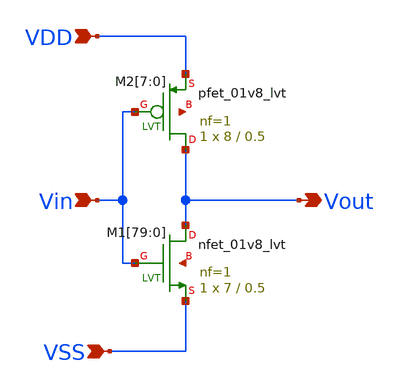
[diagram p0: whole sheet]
** sch_path: design/THESIS_EXP_RO_INVERTER_SKY130A/INV_LVT_v2.sch
**.subckt INV_LVT_v2 VDD VSS Vin Vout
*.ipin VDD
*.ipin VSS
*.ipin Vin
*.opin Vout
XM1[79] Vout Vin VSS net1[79] sky130_fd_pr__nfet_01v8_lvt L=0.5 W=7 nf=1 ad='int((nf+1)/2) * W/nf * 0.29'
+ as='int((nf+2)/2) * W/nf * 0.29' pd='2*int((nf+1)/2) * (W/nf + 0.29)' ps='2*int((nf+2)/2) * (W/nf + 0.29)'
+ nrd='0.29 / W' nrs='0.29 / W' sa=0 sb=0 sd=0 mult=1 m=1
XM1[78] Vout Vin VSS net1[78] sky130_fd_pr__nfet_01v8_lvt L=0.5 W=7 nf=1 ad='int((nf+1)/2) * W/nf * 0.29'
+ as='int((nf+2)/2) * W/nf * 0.29' pd='2*int((nf+1)/2) * (W/nf + 0.29)' ps='2*int((nf+2)/2) * (W/nf + 0.29)'
+ nrd='0.29 / W' nrs='0.29 / W' sa=0 sb=0 sd=0 mult=1 m=1
XM1[77] Vout Vin VSS net1[77] sky130_fd_pr__nfet_01v8_lvt L=0.5 W=7 nf=1 ad='int((nf+1)/2) * W/nf * 0.29'
+ as='int((nf+2)/2) * W/nf * 0.29' pd='2*int((nf+1)/2) * (W/nf + 0.29)' ps='2*int((nf+2)/2) * (W/nf + 0.29)'
+ nrd='0.29 / W' nrs='0.29 / W' sa=0 sb=0 sd=0 mult=1 m=1
XM1[76] Vout Vin VSS net1[76] sky130_fd_pr__nfet_01v8_lvt L=0.5 W=7 nf=1 ad='int((nf+1)/2) * W/nf * 0.29'
+ as='int((nf+2)/2) * W/nf * 0.29' pd='2*int((nf+1)/2) * (W/nf + 0.29)' ps='2*int((nf+2)/2) * (W/nf + 0.29)'
+ nrd='0.29 / W' nrs='0.29 / W' sa=0 sb=0 sd=0 mult=1 m=1
XM1[75] Vout Vin VSS net1[75] sky130_fd_pr__nfet_01v8_lvt L=0.5 W=7 nf=1 ad='int((nf+1)/2) * W/nf * 0.29'
+ as='int((nf+2)/2) * W/nf * 0.29' pd='2*int((nf+1)/2) * (W/nf + 0.29)' ps='2*int((nf+2)/2) * (W/nf + 0.29)'
+ nrd='0.29 / W' nrs='0.29 / W' sa=0 sb=0 sd=0 mult=1 m=1
XM1[74] Vout Vin VSS net1[74] sky130_fd_pr__nfet_01v8_lvt L=0.5 W=7 nf=1 ad='int((nf+1)/2) * W/nf * 0.29'
+ as='int((nf+2)/2) * W/nf * 0.29' pd='2*int((nf+1)/2) * (W/nf + 0.29)' ps='2*int((nf+2)/2) * (W/nf + 0.29)'
+ nrd='0.29 / W' nrs='0.29 / W' sa=0 sb=0 sd=0 mult=1 m=1
XM1[73] Vout Vin VSS net1[73] sky130_fd_pr__nfet_01v8_lvt L=0.5 W=7 nf=1 ad='int((nf+1)/2) * W/nf * 0.29'
+ as='int((nf+2)/2) * W/nf * 0.29' pd='2*int((nf+1)/2) * (W/nf + 0.29)' ps='2*int((nf+2)/2) * (W/nf + 0.29)'
+ nrd='0.29 / W' nrs='0.29 / W' sa=0 sb=0 sd=0 mult=1 m=1
XM1[72] Vout Vin VSS net1[72] sky130_fd_pr__nfet_01v8_lvt L=0.5 W=7 nf=1 ad='int((nf+1)/2) * W/nf * 0.29'
+ as='int((nf+2)/2) * W/nf * 0.29' pd='2*int((nf+1)/2) * (W/nf + 0.29)' ps='2*int((nf+2)/2) * (W/nf + 0.29)'
+ nrd='0.29 / W' nrs='0.29 / W' sa=0 sb=0 sd=0 mult=1 m=1
XM1[71] Vout Vin VSS net1[71] sky130_fd_pr__nfet_01v8_lvt L=0.5 W=7 nf=1 ad='int((nf+1)/2) * W/nf * 0.29'
+ as='int((nf+2)/2) * W/nf * 0.29' pd='2*int((nf+1)/2) * (W/nf + 0.29)' ps='2*int((nf+2)/2) * (W/nf + 0.29)'
+ nrd='0.29 / W' nrs='0.29 / W' sa=0 sb=0 sd=0 mult=1 m=1
XM1[70] Vout Vin VSS net1[70] sky130_fd_pr__nfet_01v8_lvt L=0.5 W=7 nf=1 ad='int((nf+1)/2) * W/nf * 0.29'
+ as='int((nf+2)/2) * W/nf * 0.29' pd='2*int((nf+1)/2) * (W/nf + 0.29)' ps='2*int((nf+2)/2) * (W/nf + 0.29)'
+ nrd='0.29 / W' nrs='0.29 / W' sa=0 sb=0 sd=0 mult=1 m=1
XM1[69] Vout Vin VSS net1[69] sky130_fd_pr__nfet_01v8_lvt L=0.5 W=7 nf=1 ad='int((nf+1)/2) * W/nf * 0.29'
+ as='int((nf+2)/2) * W/nf * 0.29' pd='2*int((nf+1)/2) * (W/nf + 0.29)' ps='2*int((nf+2)/2) * (W/nf + 0.29)'
+ nrd='0.29 / W' nrs='0.29 / W' sa=0 sb=0 sd=0 mult=1 m=1
XM1[68] Vout Vin VSS net1[68] sky130_fd_pr__nfet_01v8_lvt L=0.5 W=7 nf=1 ad='int((nf+1)/2) * W/nf * 0.29'
+ as='int((nf+2)/2) * W/nf * 0.29' pd='2*int((nf+1)/2) * (W/nf + 0.29)' ps='2*int((nf+2)/2) * (W/nf + 0.29)'
+ nrd='0.29 / W' nrs='0.29 / W' sa=0 sb=0 sd=0 mult=1 m=1
XM1[67] Vout Vin VSS net1[67] sky130_fd_pr__nfet_01v8_lvt L=0.5 W=7 nf=1 ad='int((nf+1)/2) * W/nf * 0.29'
+ as='int((nf+2)/2) * W/nf * 0.29' pd='2*int((nf+1)/2) * (W/nf + 0.29)' ps='2*int((nf+2)/2) * (W/nf + 0.29)'
+ nrd='0.29 / W' nrs='0.29 / W' sa=0 sb=0 sd=0 mult=1 m=1
XM1[66] Vout Vin VSS net1[66] sky130_fd_pr__nfet_01v8_lvt L=0.5 W=7 nf=1 ad='int((nf+1)/2) * W/nf * 0.29'
+ as='int((nf+2)/2) * W/nf * 0.29' pd='2*int((nf+1)/2) * (W/nf + 0.29)' ps='2*int((nf+2)/2) * (W/nf + 0.29)'
+ nrd='0.29 / W' nrs='0.29 / W' sa=0 sb=0 sd=0 mult=1 m=1
XM1[65] Vout Vin VSS net1[65] sky130_fd_pr__nfet_01v8_lvt L=0.5 W=7 nf=1 ad='int((nf+1)/2) * W/nf * 0.29'
+ as='int((nf+2)/2) * W/nf * 0.29' pd='2*int((nf+1)/2) * (W/nf + 0.29)' ps='2*int((nf+2)/2) * (W/nf + 0.29)'
+ nrd='0.29 / W' nrs='0.29 / W' sa=0 sb=0 sd=0 mult=1 m=1
XM1[64] Vout Vin VSS net1[64] sky130_fd_pr__nfet_01v8_lvt L=0.5 W=7 nf=1 ad='int((nf+1)/2) * W/nf * 0.29'
+ as='int((nf+2)/2) * W/nf * 0.29' pd='2*int((nf+1)/2) * (W/nf + 0.29)' ps='2*int((nf+2)/2) * (W/nf + 0.29)'
+ nrd='0.29 / W' nrs='0.29 / W' sa=0 sb=0 sd=0 mult=1 m=1
XM1[63] Vout Vin VSS net1[63] sky130_fd_pr__nfet_01v8_lvt L=0.5 W=7 nf=1 ad='int((nf+1)/2) * W/nf * 0.29'
+ as='int((nf+2)/2) * W/nf * 0.29' pd='2*int((nf+1)/2) * (W/nf + 0.29)' ps='2*int((nf+2)/2) * (W/nf + 0.29)'
+ nrd='0.29 / W' nrs='0.29 / W' sa=0 sb=0 sd=0 mult=1 m=1
XM1[62] Vout Vin VSS net1[62] sky130_fd_pr__nfet_01v8_lvt L=0.5 W=7 nf=1 ad='int((nf+1)/2) * W/nf * 0.29'
+ as='int((nf+2)/2) * W/nf * 0.29' pd='2*int((nf+1)/2) * (W/nf + 0.29)' ps='2*int((nf+2)/2) * (W/nf + 0.29)'
+ nrd='0.29 / W' nrs='0.29 / W' sa=0 sb=0 sd=0 mult=1 m=1
XM1[61] Vout Vin VSS net1[61] sky130_fd_pr__nfet_01v8_lvt L=0.5 W=7 nf=1 ad='int((nf+1)/2) * W/nf * 0.29'
+ as='int((nf+2)/2) * W/nf * 0.29' pd='2*int((nf+1)/2) * (W/nf + 0.29)' ps='2*int((nf+2)/2) * (W/nf + 0.29)'
+ nrd='0.29 / W' nrs='0.29 / W' sa=0 sb=0 sd=0 mult=1 m=1
XM1[60] Vout Vin VSS net1[60] sky130_fd_pr__nfet_01v8_lvt L=0.5 W=7 nf=1 ad='int((nf+1)/2) * W/nf * 0.29'
+ as='int((nf+2)/2) * W/nf * 0.29' pd='2*int((nf+1)/2) * (W/nf + 0.29)' ps='2*int((nf+2)/2) * (W/nf + 0.29)'
+ nrd='0.29 / W' nrs='0.29 / W' sa=0 sb=0 sd=0 mult=1 m=1
XM1[59] Vout Vin VSS net1[59] sky130_fd_pr__nfet_01v8_lvt L=0.5 W=7 nf=1 ad='int((nf+1)/2) * W/nf * 0.29'
+ as='int((nf+2)/2) * W/nf * 0.29' pd='2*int((nf+1)/2) * (W/nf + 0.29)' ps='2*int((nf+2)/2) * (W/nf + 0.29)'
+ nrd='0.29 / W' nrs='0.29 / W' sa=0 sb=0 sd=0 mult=1 m=1
XM1[58] Vout Vin VSS net1[58] sky130_fd_pr__nfet_01v8_lvt L=0.5 W=7 nf=1 ad='int((nf+1)/2) * W/nf * 0.29'
+ as='int((nf+2)/2) * W/nf * 0.29' pd='2*int((nf+1)/2) * (W/nf + 0.29)' ps='2*int((nf+2)/2) * (W/nf + 0.29)'
+ nrd='0.29 / W' nrs='0.29 / W' sa=0 sb=0 sd=0 mult=1 m=1
XM1[57] Vout Vin VSS net1[57] sky130_fd_pr__nfet_01v8_lvt L=0.5 W=7 nf=1 ad='int((nf+1)/2) * W/nf * 0.29'
+ as='int((nf+2)/2) * W/nf * 0.29' pd='2*int((nf+1)/2) * (W/nf + 0.29)' ps='2*int((nf+2)/2) * (W/nf + 0.29)'
+ nrd='0.29 / W' nrs='0.29 / W' sa=0 sb=0 sd=0 mult=1 m=1
XM1[56] Vout Vin VSS net1[56] sky130_fd_pr__nfet_01v8_lvt L=0.5 W=7 nf=1 ad='int((nf+1)/2) * W/nf * 0.29'
+ as='int((nf+2)/2) * W/nf * 0.29' pd='2*int((nf+1)/2) * (W/nf + 0.29)' ps='2*int((nf+2)/2) * (W/nf + 0.29)'
+ nrd='0.29 / W' nrs='0.29 / W' sa=0 sb=0 sd=0 mult=1 m=1
XM1[55] Vout Vin VSS net1[55] sky130_fd_pr__nfet_01v8_lvt L=0.5 W=7 nf=1 ad='int((nf+1)/2) * W/nf * 0.29'
+ as='int((nf+2)/2) * W/nf * 0.29' pd='2*int((nf+1)/2) * (W/nf + 0.29)' ps='2*int((nf+2)/2) * (W/nf + 0.29)'
+ nrd='0.29 / W' nrs='0.29 / W' sa=0 sb=0 sd=0 mult=1 m=1
XM1[54] Vout Vin VSS net1[54] sky130_fd_pr__nfet_01v8_lvt L=0.5 W=7 nf=1 ad='int((nf+1)/2) * W/nf * 0.29'
+ as='int((nf+2)/2) * W/nf * 0.29' pd='2*int((nf+1)/2) * (W/nf + 0.29)' ps='2*int((nf+2)/2) * (W/nf + 0.29)'
+ nrd='0.29 / W' nrs='0.29 / W' sa=0 sb=0 sd=0 mult=1 m=1
XM1[53] Vout Vin VSS net1[53] sky130_fd_pr__nfet_01v8_lvt L=0.5 W=7 nf=1 ad='int((nf+1)/2) * W/nf * 0.29'
+ as='int((nf+2)/2) * W/nf * 0.29' pd='2*int((nf+1)/2) * (W/nf + 0.29)' ps='2*int((nf+2)/2) * (W/nf + 0.29)'
+ nrd='0.29 / W' nrs='0.29 / W' sa=0 sb=0 sd=0 mult=1 m=1
XM1[52] Vout Vin VSS net1[52] sky130_fd_pr__nfet_01v8_lvt L=0.5 W=7 nf=1 ad='int((nf+1)/2) * W/nf * 0.29'
+ as='int((nf+2)/2) * W/nf * 0.29' pd='2*int((nf+1)/2) * (W/nf + 0.29)' ps='2*int((nf+2)/2) * (W/nf + 0.29)'
+ nrd='0.29 / W' nrs='0.29 / W' sa=0 sb=0 sd=0 mult=1 m=1
XM1[51] Vout Vin VSS net1[51] sky130_fd_pr__nfet_01v8_lvt L=0.5 W=7 nf=1 ad='int((nf+1)/2) * W/nf * 0.29'
+ as='int((nf+2)/2) * W/nf * 0.29' pd='2*int((nf+1)/2) * (W/nf + 0.29)' ps='2*int((nf+2)/2) * (W/nf + 0.29)'
+ nrd='0.29 / W' nrs='0.29 / W' sa=0 sb=0 sd=0 mult=1 m=1
XM1[50] Vout Vin VSS net1[50] sky130_fd_pr__nfet_01v8_lvt L=0.5 W=7 nf=1 ad='int((nf+1)/2) * W/nf * 0.29'
+ as='int((nf+2)/2) * W/nf * 0.29' pd='2*int((nf+1)/2) * (W/nf + 0.29)' ps='2*int((nf+2)/2) * (W/nf + 0.29)'
+ nrd='0.29 / W' nrs='0.29 / W' sa=0 sb=0 sd=0 mult=1 m=1
XM1[49] Vout Vin VSS net1[49] sky130_fd_pr__nfet_01v8_lvt L=0.5 W=7 nf=1 ad='int((nf+1)/2) * W/nf * 0.29'
+ as='int((nf+2)/2) * W/nf * 0.29' pd='2*int((nf+1)/2) * (W/nf + 0.29)' ps='2*int((nf+2)/2) * (W/nf + 0.29)'
+ nrd='0.29 / W' nrs='0.29 / W' sa=0 sb=0 sd=0 mult=1 m=1
XM1[48] Vout Vin VSS net1[48] sky130_fd_pr__nfet_01v8_lvt L=0.5 W=7 nf=1 ad='int((nf+1)/2) * W/nf * 0.29'
+ as='int((nf+2)/2) * W/nf * 0.29' pd='2*int((nf+1)/2) * (W/nf + 0.29)' ps='2*int((nf+2)/2) * (W/nf + 0.29)'
+ nrd='0.29 / W' nrs='0.29 / W' sa=0 sb=0 sd=0 mult=1 m=1
XM1[47] Vout Vin VSS net1[47] sky130_fd_pr__nfet_01v8_lvt L=0.5 W=7 nf=1 ad='int((nf+1)/2) * W/nf * 0.29'
+ as='int((nf+2)/2) * W/nf * 0.29' pd='2*int((nf+1)/2) * (W/nf + 0.29)' ps='2*int((nf+2)/2) * (W/nf + 0.29)'
+ nrd='0.29 / W' nrs='0.29 / W' sa=0 sb=0 sd=0 mult=1 m=1
XM1[46] Vout Vin VSS net1[46] sky130_fd_pr__nfet_01v8_lvt L=0.5 W=7 nf=1 ad='int((nf+1)/2) * W/nf * 0.29'
+ as='int((nf+2)/2) * W/nf * 0.29' pd='2*int((nf+1)/2) * (W/nf + 0.29)' ps='2*int((nf+2)/2) * (W/nf + 0.29)'
+ nrd='0.29 / W' nrs='0.29 / W' sa=0 sb=0 sd=0 mult=1 m=1
XM1[45] Vout Vin VSS net1[45] sky130_fd_pr__nfet_01v8_lvt L=0.5 W=7 nf=1 ad='int((nf+1)/2) * W/nf * 0.29'
+ as='int((nf+2)/2) * W/nf * 0.29' pd='2*int((nf+1)/2) * (W/nf + 0.29)' ps='2*int((nf+2)/2) * (W/nf + 0.29)'
+ nrd='0.29 / W' nrs='0.29 / W' sa=0 sb=0 sd=0 mult=1 m=1
XM1[44] Vout Vin VSS net1[44] sky130_fd_pr__nfet_01v8_lvt L=0.5 W=7 nf=1 ad='int((nf+1)/2) * W/nf * 0.29'
+ as='int((nf+2)/2) * W/nf * 0.29' pd='2*int((nf+1)/2) * (W/nf + 0.29)' ps='2*int((nf+2)/2) * (W/nf + 0.29)'
+ nrd='0.29 / W' nrs='0.29 / W' sa=0 sb=0 sd=0 mult=1 m=1
XM1[43] Vout Vin VSS net1[43] sky130_fd_pr__nfet_01v8_lvt L=0.5 W=7 nf=1 ad='int((nf+1)/2) * W/nf * 0.29'
+ as='int((nf+2)/2) * W/nf * 0.29' pd='2*int((nf+1)/2) * (W/nf + 0.29)' ps='2*int((nf+2)/2) * (W/nf + 0.29)'
+ nrd='0.29 / W' nrs='0.29 / W' sa=0 sb=0 sd=0 mult=1 m=1
XM1[42] Vout Vin VSS net1[42] sky130_fd_pr__nfet_01v8_lvt L=0.5 W=7 nf=1 ad='int((nf+1)/2) * W/nf * 0.29'
+ as='int((nf+2)/2) * W/nf * 0.29' pd='2*int((nf+1)/2) * (W/nf + 0.29)' ps='2*int((nf+2)/2) * (W/nf + 0.29)'
+ nrd='0.29 / W' nrs='0.29 / W' sa=0 sb=0 sd=0 mult=1 m=1
XM1[41] Vout Vin VSS net1[41] sky130_fd_pr__nfet_01v8_lvt L=0.5 W=7 nf=1 ad='int((nf+1)/2) * W/nf * 0.29'
+ as='int((nf+2)/2) * W/nf * 0.29' pd='2*int((nf+1)/2) * (W/nf + 0.29)' ps='2*int((nf+2)/2) * (W/nf + 0.29)'
+ nrd='0.29 / W' nrs='0.29 / W' sa=0 sb=0 sd=0 mult=1 m=1
XM1[40] Vout Vin VSS net1[40] sky130_fd_pr__nfet_01v8_lvt L=0.5 W=7 nf=1 ad='int((nf+1)/2) * W/nf * 0.29'
+ as='int((nf+2)/2) * W/nf * 0.29' pd='2*int((nf+1)/2) * (W/nf + 0.29)' ps='2*int((nf+2)/2) * (W/nf + 0.29)'
+ nrd='0.29 / W' nrs='0.29 / W' sa=0 sb=0 sd=0 mult=1 m=1
XM1[39] Vout Vin VSS net1[39] sky130_fd_pr__nfet_01v8_lvt L=0.5 W=7 nf=1 ad='int((nf+1)/2) * W/nf * 0.29'
+ as='int((nf+2)/2) * W/nf * 0.29' pd='2*int((nf+1)/2) * (W/nf + 0.29)' ps='2*int((nf+2)/2) * (W/nf + 0.29)'
+ nrd='0.29 / W' nrs='0.29 / W' sa=0 sb=0 sd=0 mult=1 m=1
XM1[38] Vout Vin VSS net1[38] sky130_fd_pr__nfet_01v8_lvt L=0.5 W=7 nf=1 ad='int((nf+1)/2) * W/nf * 0.29'
+ as='int((nf+2)/2) * W/nf * 0.29' pd='2*int((nf+1)/2) * (W/nf + 0.29)' ps='2*int((nf+2)/2) * (W/nf + 0.29)'
+ nrd='0.29 / W' nrs='0.29 / W' sa=0 sb=0 sd=0 mult=1 m=1
XM1[37] Vout Vin VSS net1[37] sky130_fd_pr__nfet_01v8_lvt L=0.5 W=7 nf=1 ad='int((nf+1)/2) * W/nf * 0.29'
+ as='int((nf+2)/2) * W/nf * 0.29' pd='2*int((nf+1)/2) * (W/nf + 0.29)' ps='2*int((nf+2)/2) * (W/nf + 0.29)'
+ nrd='0.29 / W' nrs='0.29 / W' sa=0 sb=0 sd=0 mult=1 m=1
XM1[36] Vout Vin VSS net1[36] sky130_fd_pr__nfet_01v8_lvt L=0.5 W=7 nf=1 ad='int((nf+1)/2) * W/nf * 0.29'
+ as='int((nf+2)/2) * W/nf * 0.29' pd='2*int((nf+1)/2) * (W/nf + 0.29)' ps='2*int((nf+2)/2) * (W/nf + 0.29)'
+ nrd='0.29 / W' nrs='0.29 / W' sa=0 sb=0 sd=0 mult=1 m=1
XM1[35] Vout Vin VSS net1[35] sky130_fd_pr__nfet_01v8_lvt L=0.5 W=7 nf=1 ad='int((nf+1)/2) * W/nf * 0.29'
+ as='int((nf+2)/2) * W/nf * 0.29' pd='2*int((nf+1)/2) * (W/nf + 0.29)' ps='2*int((nf+2)/2) * (W/nf + 0.29)'
+ nrd='0.29 / W' nrs='0.29 / W' sa=0 sb=0 sd=0 mult=1 m=1
XM1[34] Vout Vin VSS net1[34] sky130_fd_pr__nfet_01v8_lvt L=0.5 W=7 nf=1 ad='int((nf+1)/2) * W/nf * 0.29'
+ as='int((nf+2)/2) * W/nf * 0.29' pd='2*int((nf+1)/2) * (W/nf + 0.29)' ps='2*int((nf+2)/2) * (W/nf + 0.29)'
+ nrd='0.29 / W' nrs='0.29 / W' sa=0 sb=0 sd=0 mult=1 m=1
XM1[33] Vout Vin VSS net1[33] sky130_fd_pr__nfet_01v8_lvt L=0.5 W=7 nf=1 ad='int((nf+1)/2) * W/nf * 0.29'
+ as='int((nf+2)/2) * W/nf * 0.29' pd='2*int((nf+1)/2) * (W/nf + 0.29)' ps='2*int((nf+2)/2) * (W/nf + 0.29)'
+ nrd='0.29 / W' nrs='0.29 / W' sa=0 sb=0 sd=0 mult=1 m=1
XM1[32] Vout Vin VSS net1[32] sky130_fd_pr__nfet_01v8_lvt L=0.5 W=7 nf=1 ad='int((nf+1)/2) * W/nf * 0.29'
+ as='int((nf+2)/2) * W/nf * 0.29' pd='2*int((nf+1)/2) * (W/nf + 0.29)' ps='2*int((nf+2)/2) * (W/nf + 0.29)'
+ nrd='0.29 / W' nrs='0.29 / W' sa=0 sb=0 sd=0 mult=1 m=1
XM1[31] Vout Vin VSS net1[31] sky130_fd_pr__nfet_01v8_lvt L=0.5 W=7 nf=1 ad='int((nf+1)/2) * W/nf * 0.29'
+ as='int((nf+2)/2) * W/nf * 0.29' pd='2*int((nf+1)/2) * (W/nf + 0.29)' ps='2*int((nf+2)/2) * (W/nf + 0.29)'
+ nrd='0.29 / W' nrs='0.29 / W' sa=0 sb=0 sd=0 mult=1 m=1
XM1[30] Vout Vin VSS net1[30] sky130_fd_pr__nfet_01v8_lvt L=0.5 W=7 nf=1 ad='int((nf+1)/2) * W/nf * 0.29'
+ as='int((nf+2)/2) * W/nf * 0.29' pd='2*int((nf+1)/2) * (W/nf + 0.29)' ps='2*int((nf+2)/2) * (W/nf + 0.29)'
+ nrd='0.29 / W' nrs='0.29 / W' sa=0 sb=0 sd=0 mult=1 m=1
XM1[29] Vout Vin VSS net1[29] sky130_fd_pr__nfet_01v8_lvt L=0.5 W=7 nf=1 ad='int((nf+1)/2) * W/nf * 0.29'
+ as='int((nf+2)/2) * W/nf * 0.29' pd='2*int((nf+1)/2) * (W/nf + 0.29)' ps='2*int((nf+2)/2) * (W/nf + 0.29)'
+ nrd='0.29 / W' nrs='0.29 / W' sa=0 sb=0 sd=0 mult=1 m=1
XM1[28] Vout Vin VSS net1[28] sky130_fd_pr__nfet_01v8_lvt L=0.5 W=7 nf=1 ad='int((nf+1)/2) * W/nf * 0.29'
+ as='int((nf+2)/2) * W/nf * 0.29' pd='2*int((nf+1)/2) * (W/nf + 0.29)' ps='2*int((nf+2)/2) * (W/nf + 0.29)'
+ nrd='0.29 / W' nrs='0.29 / W' sa=0 sb=0 sd=0 mult=1 m=1
XM1[27] Vout Vin VSS net1[27] sky130_fd_pr__nfet_01v8_lvt L=0.5 W=7 nf=1 ad='int((nf+1)/2) * W/nf * 0.29'
+ as='int((nf+2)/2) * W/nf * 0.29' pd='2*int((nf+1)/2) * (W/nf + 0.29)' ps='2*int((nf+2)/2) * (W/nf + 0.29)'
+ nrd='0.29 / W' nrs='0.29 / W' sa=0 sb=0 sd=0 mult=1 m=1
XM1[26] Vout Vin VSS net1[26] sky130_fd_pr__nfet_01v8_lvt L=0.5 W=7 nf=1 ad='int((nf+1)/2) * W/nf * 0.29'
+ as='int((nf+2)/2) * W/nf * 0.29' pd='2*int((nf+1)/2) * (W/nf + 0.29)' ps='2*int((nf+2)/2) * (W/nf + 0.29)'
+ nrd='0.29 / W' nrs='0.29 / W' sa=0 sb=0 sd=0 mult=1 m=1
XM1[25] Vout Vin VSS net1[25] sky130_fd_pr__nfet_01v8_lvt L=0.5 W=7 nf=1 ad='int((nf+1)/2) * W/nf * 0.29'
+ as='int((nf+2)/2) * W/nf * 0.29' pd='2*int((nf+1)/2) * (W/nf + 0.29)' ps='2*int((nf+2)/2) * (W/nf + 0.29)'
+ nrd='0.29 / W' nrs='0.29 / W' sa=0 sb=0 sd=0 mult=1 m=1
XM1[24] Vout Vin VSS net1[24] sky130_fd_pr__nfet_01v8_lvt L=0.5 W=7 nf=1 ad='int((nf+1)/2) * W/nf * 0.29'
+ as='int((nf+2)/2) * W/nf * 0.29' pd='2*int((nf+1)/2) * (W/nf + 0.29)' ps='2*int((nf+2)/2) * (W/nf + 0.29)'
+ nrd='0.29 / W' nrs='0.29 / W' sa=0 sb=0 sd=0 mult=1 m=1
XM1[23] Vout Vin VSS net1[23] sky130_fd_pr__nfet_01v8_lvt L=0.5 W=7 nf=1 ad='int((nf+1)/2) * W/nf * 0.29'
+ as='int((nf+2)/2) * W/nf * 0.29' pd='2*int((nf+1)/2) * (W/nf + 0.29)' ps='2*int((nf+2)/2) * (W/nf + 0.29)'
+ nrd='0.29 / W' nrs='0.29 / W' sa=0 sb=0 sd=0 mult=1 m=1
XM1[22] Vout Vin VSS net1[22] sky130_fd_pr__nfet_01v8_lvt L=0.5 W=7 nf=1 ad='int((nf+1)/2) * W/nf * 0.29'
+ as='int((nf+2)/2) * W/nf * 0.29' pd='2*int((nf+1)/2) * (W/nf + 0.29)' ps='2*int((nf+2)/2) * (W/nf + 0.29)'
+ nrd='0.29 / W' nrs='0.29 / W' sa=0 sb=0 sd=0 mult=1 m=1
XM1[21] Vout Vin VSS net1[21] sky130_fd_pr__nfet_01v8_lvt L=0.5 W=7 nf=1 ad='int((nf+1)/2) * W/nf * 0.29'
+ as='int((nf+2)/2) * W/nf * 0.29' pd='2*int((nf+1)/2) * (W/nf + 0.29)' ps='2*int((nf+2)/2) * (W/nf + 0.29)'
+ nrd='0.29 / W' nrs='0.29 / W' sa=0 sb=0 sd=0 mult=1 m=1
XM1[20] Vout Vin VSS net1[20] sky130_fd_pr__nfet_01v8_lvt L=0.5 W=7 nf=1 ad='int((nf+1)/2) * W/nf * 0.29'
+ as='int((nf+2)/2) * W/nf * 0.29' pd='2*int((nf+1)/2) * (W/nf + 0.29)' ps='2*int((nf+2)/2) * (W/nf + 0.29)'
+ nrd='0.29 / W' nrs='0.29 / W' sa=0 sb=0 sd=0 mult=1 m=1
XM1[19] Vout Vin VSS net1[19] sky130_fd_pr__nfet_01v8_lvt L=0.5 W=7 nf=1 ad='int((nf+1)/2) * W/nf * 0.29'
+ as='int((nf+2)/2) * W/nf * 0.29' pd='2*int((nf+1)/2) * (W/nf + 0.29)' ps='2*int((nf+2)/2) * (W/nf + 0.29)'
+ nrd='0.29 / W' nrs='0.29 / W' sa=0 sb=0 sd=0 mult=1 m=1
XM1[18] Vout Vin VSS net1[18] sky130_fd_pr__nfet_01v8_lvt L=0.5 W=7 nf=1 ad='int((nf+1)/2) * W/nf * 0.29'
+ as='int((nf+2)/2) * W/nf * 0.29' pd='2*int((nf+1)/2) * (W/nf + 0.29)' ps='2*int((nf+2)/2) * (W/nf + 0.29)'
+ nrd='0.29 / W' nrs='0.29 / W' sa=0 sb=0 sd=0 mult=1 m=1
XM1[17] Vout Vin VSS net1[17] sky130_fd_pr__nfet_01v8_lvt L=0.5 W=7 nf=1 ad='int((nf+1)/2) * W/nf * 0.29'
+ as='int((nf+2)/2) * W/nf * 0.29' pd='2*int((nf+1)/2) * (W/nf + 0.29)' ps='2*int((nf+2)/2) * (W/nf + 0.29)'
+ nrd='0.29 / W' nrs='0.29 / W' sa=0 sb=0 sd=0 mult=1 m=1
XM1[16] Vout Vin VSS net1[16] sky130_fd_pr__nfet_01v8_lvt L=0.5 W=7 nf=1 ad='int((nf+1)/2) * W/nf * 0.29'
+ as='int((nf+2)/2) * W/nf * 0.29' pd='2*int((nf+1)/2) * (W/nf + 0.29)' ps='2*int((nf+2)/2) * (W/nf + 0.29)'
+ nrd='0.29 / W' nrs='0.29 / W' sa=0 sb=0 sd=0 mult=1 m=1
XM1[15] Vout Vin VSS net1[15] sky130_fd_pr__nfet_01v8_lvt L=0.5 W=7 nf=1 ad='int((nf+1)/2) * W/nf * 0.29'
+ as='int((nf+2)/2) * W/nf * 0.29' pd='2*int((nf+1)/2) * (W/nf + 0.29)' ps='2*int((nf+2)/2) * (W/nf + 0.29)'
+ nrd='0.29 / W' nrs='0.29 / W' sa=0 sb=0 sd=0 mult=1 m=1
XM1[14] Vout Vin VSS net1[14] sky130_fd_pr__nfet_01v8_lvt L=0.5 W=7 nf=1 ad='int((nf+1)/2) * W/nf * 0.29'
+ as='int((nf+2)/2) * W/nf * 0.29' pd='2*int((nf+1)/2) * (W/nf + 0.29)' ps='2*int((nf+2)/2) * (W/nf + 0.29)'
+ nrd='0.29 / W' nrs='0.29 / W' sa=0 sb=0 sd=0 mult=1 m=1
XM1[13] Vout Vin VSS net1[13] sky130_fd_pr__nfet_01v8_lvt L=0.5 W=7 nf=1 ad='int((nf+1)/2) * W/nf * 0.29'
+ as='int((nf+2)/2) * W/nf * 0.29' pd='2*int((nf+1)/2) * (W/nf + 0.29)' ps='2*int((nf+2)/2) * (W/nf + 0.29)'
+ nrd='0.29 / W' nrs='0.29 / W' sa=0 sb=0 sd=0 mult=1 m=1
XM1[12] Vout Vin VSS net1[12] sky130_fd_pr__nfet_01v8_lvt L=0.5 W=7 nf=1 ad='int((nf+1)/2) * W/nf * 0.29'
+ as='int((nf+2)/2) * W/nf * 0.29' pd='2*int((nf+1)/2) * (W/nf + 0.29)' ps='2*int((nf+2)/2) * (W/nf + 0.29)'
+ nrd='0.29 / W' nrs='0.29 / W' sa=0 sb=0 sd=0 mult=1 m=1
XM1[11] Vout Vin VSS net1[11] sky130_fd_pr__nfet_01v8_lvt L=0.5 W=7 nf=1 ad='int((nf+1)/2) * W/nf * 0.29'
+ as='int((nf+2)/2) * W/nf * 0.29' pd='2*int((nf+1)/2) * (W/nf + 0.29)' ps='2*int((nf+2)/2) * (W/nf + 0.29)'
+ nrd='0.29 / W' nrs='0.29 / W' sa=0 sb=0 sd=0 mult=1 m=1
XM1[10] Vout Vin VSS net1[10] sky130_fd_pr__nfet_01v8_lvt L=0.5 W=7 nf=1 ad='int((nf+1)/2) * W/nf * 0.29'
+ as='int((nf+2)/2) * W/nf * 0.29' pd='2*int((nf+1)/2) * (W/nf + 0.29)' ps='2*int((nf+2)/2) * (W/nf + 0.29)'
+ nrd='0.29 / W' nrs='0.29 / W' sa=0 sb=0 sd=0 mult=1 m=1
XM1[9] Vout Vin VSS net1[9] sky130_fd_pr__nfet_01v8_lvt L=0.5 W=7 nf=1 ad='int((nf+1)/2) * W/nf * 0.29'
+ as='int((nf+2)/2) * W/nf * 0.29' pd='2*int((nf+1)/2) * (W/nf + 0.29)' ps='2*int((nf+2)/2) * (W/nf + 0.29)'
+ nrd='0.29 / W' nrs='0.29 / W' sa=0 sb=0 sd=0 mult=1 m=1
XM1[8] Vout Vin VSS net1[8] sky130_fd_pr__nfet_01v8_lvt L=0.5 W=7 nf=1 ad='int((nf+1)/2) * W/nf * 0.29'
+ as='int((nf+2)/2) * W/nf * 0.29' pd='2*int((nf+1)/2) * (W/nf + 0.29)' ps='2*int((nf+2)/2) * (W/nf + 0.29)'
+ nrd='0.29 / W' nrs='0.29 / W' sa=0 sb=0 sd=0 mult=1 m=1
XM1[7] Vout Vin VSS net1[7] sky130_fd_pr__nfet_01v8_lvt L=0.5 W=7 nf=1 ad='int((nf+1)/2) * W/nf * 0.29'
+ as='int((nf+2)/2) * W/nf * 0.29' pd='2*int((nf+1)/2) * (W/nf + 0.29)' ps='2*int((nf+2)/2) * (W/nf + 0.29)'
+ nrd='0.29 / W' nrs='0.29 / W' sa=0 sb=0 sd=0 mult=1 m=1
XM1[6] Vout Vin VSS net1[6] sky130_fd_pr__nfet_01v8_lvt L=0.5 W=7 nf=1 ad='int((nf+1)/2) * W/nf * 0.29'
+ as='int((nf+2)/2) * W/nf * 0.29' pd='2*int((nf+1)/2) * (W/nf + 0.29)' ps='2*int((nf+2)/2) * (W/nf + 0.29)'
+ nrd='0.29 / W' nrs='0.29 / W' sa=0 sb=0 sd=0 mult=1 m=1
XM1[5] Vout Vin VSS net1[5] sky130_fd_pr__nfet_01v8_lvt L=0.5 W=7 nf=1 ad='int((nf+1)/2) * W/nf * 0.29'
+ as='int((nf+2)/2) * W/nf * 0.29' pd='2*int((nf+1)/2) * (W/nf + 0.29)' ps='2*int((nf+2)/2) * (W/nf + 0.29)'
+ nrd='0.29 / W' nrs='0.29 / W' sa=0 sb=0 sd=0 mult=1 m=1
XM1[4] Vout Vin VSS net1[4] sky130_fd_pr__nfet_01v8_lvt L=0.5 W=7 nf=1 ad='int((nf+1)/2) * W/nf * 0.29'
+ as='int((nf+2)/2) * W/nf * 0.29' pd='2*int((nf+1)/2) * (W/nf + 0.29)' ps='2*int((nf+2)/2) * (W/nf + 0.29)'
+ nrd='0.29 / W' nrs='0.29 / W' sa=0 sb=0 sd=0 mult=1 m=1
XM1[3] Vout Vin VSS net1[3] sky130_fd_pr__nfet_01v8_lvt L=0.5 W=7 nf=1 ad='int((nf+1)/2) * W/nf * 0.29'
+ as='int((nf+2)/2) * W/nf * 0.29' pd='2*int((nf+1)/2) * (W/nf + 0.29)' ps='2*int((nf+2)/2) * (W/nf + 0.29)'
+ nrd='0.29 / W' nrs='0.29 / W' sa=0 sb=0 sd=0 mult=1 m=1
XM1[2] Vout Vin VSS net1[2] sky130_fd_pr__nfet_01v8_lvt L=0.5 W=7 nf=1 ad='int((nf+1)/2) * W/nf * 0.29'
+ as='int((nf+2)/2) * W/nf * 0.29' pd='2*int((nf+1)/2) * (W/nf + 0.29)' ps='2*int((nf+2)/2) * (W/nf + 0.29)'
+ nrd='0.29 / W' nrs='0.29 / W' sa=0 sb=0 sd=0 mult=1 m=1
XM1[1] Vout Vin VSS net1[1] sky130_fd_pr__nfet_01v8_lvt L=0.5 W=7 nf=1 ad='int((nf+1)/2) * W/nf * 0.29'
+ as='int((nf+2)/2) * W/nf * 0.29' pd='2*int((nf+1)/2) * (W/nf + 0.29)' ps='2*int((nf+2)/2) * (W/nf + 0.29)'
+ nrd='0.29 / W' nrs='0.29 / W' sa=0 sb=0 sd=0 mult=1 m=1
XM1[0] Vout Vin VSS net1[0] sky130_fd_pr__nfet_01v8_lvt L=0.5 W=7 nf=1 ad='int((nf+1)/2) * W/nf * 0.29'
+ as='int((nf+2)/2) * W/nf * 0.29' pd='2*int((nf+1)/2) * (W/nf + 0.29)' ps='2*int((nf+2)/2) * (W/nf + 0.29)'
+ nrd='0.29 / W' nrs='0.29 / W' sa=0 sb=0 sd=0 mult=1 m=1
XM2[7] Vout Vin VDD net2[7] sky130_fd_pr__pfet_01v8_lvt L=0.5 W=8 nf=1 ad='int((nf+1)/2) * W/nf * 0.29'
+ as='int((nf+2)/2) * W/nf * 0.29' pd='2*int((nf+1)/2) * (W/nf + 0.29)' ps='2*int((nf+2)/2) * (W/nf + 0.29)'
+ nrd='0.29 / W' nrs='0.29 / W' sa=0 sb=0 sd=0 mult=1 m=1
XM2[6] Vout Vin VDD net2[6] sky130_fd_pr__pfet_01v8_lvt L=0.5 W=8 nf=1 ad='int((nf+1)/2) * W/nf * 0.29'
+ as='int((nf+2)/2) * W/nf * 0.29' pd='2*int((nf+1)/2) * (W/nf + 0.29)' ps='2*int((nf+2)/2) * (W/nf + 0.29)'
+ nrd='0.29 / W' nrs='0.29 / W' sa=0 sb=0 sd=0 mult=1 m=1
XM2[5] Vout Vin VDD net2[5] sky130_fd_pr__pfet_01v8_lvt L=0.5 W=8 nf=1 ad='int((nf+1)/2) * W/nf * 0.29'
+ as='int((nf+2)/2) * W/nf * 0.29' pd='2*int((nf+1)/2) * (W/nf + 0.29)' ps='2*int((nf+2)/2) * (W/nf + 0.29)'
+ nrd='0.29 / W' nrs='0.29 / W' sa=0 sb=0 sd=0 mult=1 m=1
XM2[4] Vout Vin VDD net2[4] sky130_fd_pr__pfet_01v8_lvt L=0.5 W=8 nf=1 ad='int((nf+1)/2) * W/nf * 0.29'
+ as='int((nf+2)/2) * W/nf * 0.29' pd='2*int((nf+1)/2) * (W/nf + 0.29)' ps='2*int((nf+2)/2) * (W/nf + 0.29)'
+ nrd='0.29 / W' nrs='0.29 / W' sa=0 sb=0 sd=0 mult=1 m=1
XM2[3] Vout Vin VDD net2[3] sky130_fd_pr__pfet_01v8_lvt L=0.5 W=8 nf=1 ad='int((nf+1)/2) * W/nf * 0.29'
+ as='int((nf+2)/2) * W/nf * 0.29' pd='2*int((nf+1)/2) * (W/nf + 0.29)' ps='2*int((nf+2)/2) * (W/nf + 0.29)'
+ nrd='0.29 / W' nrs='0.29 / W' sa=0 sb=0 sd=0 mult=1 m=1
XM2[2] Vout Vin VDD net2[2] sky130_fd_pr__pfet_01v8_lvt L=0.5 W=8 nf=1 ad='int((nf+1)/2) * W/nf * 0.29'
+ as='int((nf+2)/2) * W/nf * 0.29' pd='2*int((nf+1)/2) * (W/nf + 0.29)' ps='2*int((nf+2)/2) * (W/nf + 0.29)'
+ nrd='0.29 / W' nrs='0.29 / W' sa=0 sb=0 sd=0 mult=1 m=1
XM2[1] Vout Vin VDD net2[1] sky130_fd_pr__pfet_01v8_lvt L=0.5 W=8 nf=1 ad='int((nf+1)/2) * W/nf * 0.29'
+ as='int((nf+2)/2) * W/nf * 0.29' pd='2*int((nf+1)/2) * (W/nf + 0.29)' ps='2*int((nf+2)/2) * (W/nf + 0.29)'
+ nrd='0.29 / W' nrs='0.29 / W' sa=0 sb=0 sd=0 mult=1 m=1
XM2[0] Vout Vin VDD net2[0] sky130_fd_pr__pfet_01v8_lvt L=0.5 W=8 nf=1 ad='int((nf+1)/2) * W/nf * 0.29'
+ as='int((nf+2)/2) * W/nf * 0.29' pd='2*int((nf+1)/2) * (W/nf + 0.29)' ps='2*int((nf+2)/2) * (W/nf + 0.29)'
+ nrd='0.29 / W' nrs='0.29 / W' sa=0 sb=0 sd=0 mult=1 m=1
**.ends
.end
